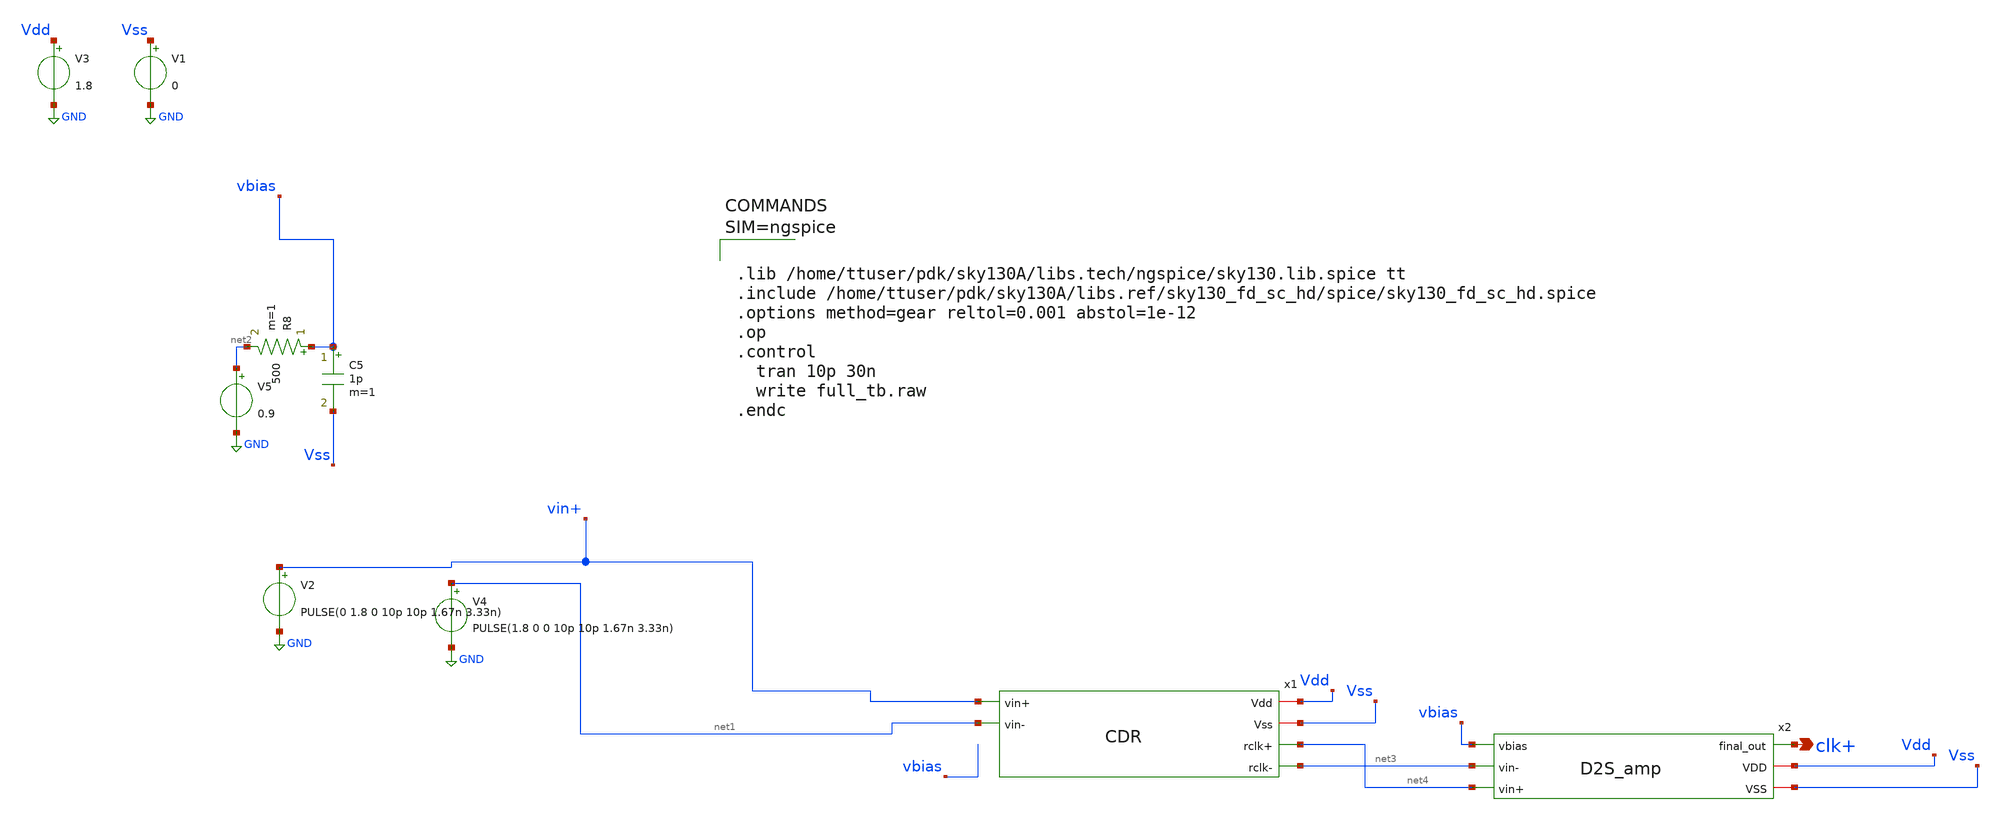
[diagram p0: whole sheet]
** sch_path: xschem/attic/full_tb.sch
**.subckt full_tb clk+
*.opin clk+
V3 Vdd GND 1.8
V1 Vss GND 0
V2 vin+ GND PULSE(0 1.8 0 10p 10p 1.67n 3.33n)
V4 net1 GND PULSE(1.8 0 0 10p 10p 1.67n 3.33n)
V5 net2 GND 0.9
R8 vbias net2 500 m=1
C5 vbias Vss 1p m=1
x1 Vdd vin+ Vss net1 net4 net3 CDR
x2 vbias net3 net4 clk+ Vdd Vss D2S_amp
**** begin user architecture code



.lib /home/ttuser/pdk/sky130A/libs.tech/ngspice/sky130.lib.spice tt
.include /home/ttuser/pdk/sky130A/libs.ref/sky130_fd_sc_hd/spice/sky130_fd_sc_hd.spice
.options method=gear reltol=0.001 abstol=1e-12
.op
.control
  tran 10p 30n
  write full_tb.raw
.endc



**** end user architecture code
**.ends
.GLOBAL GND
.end
